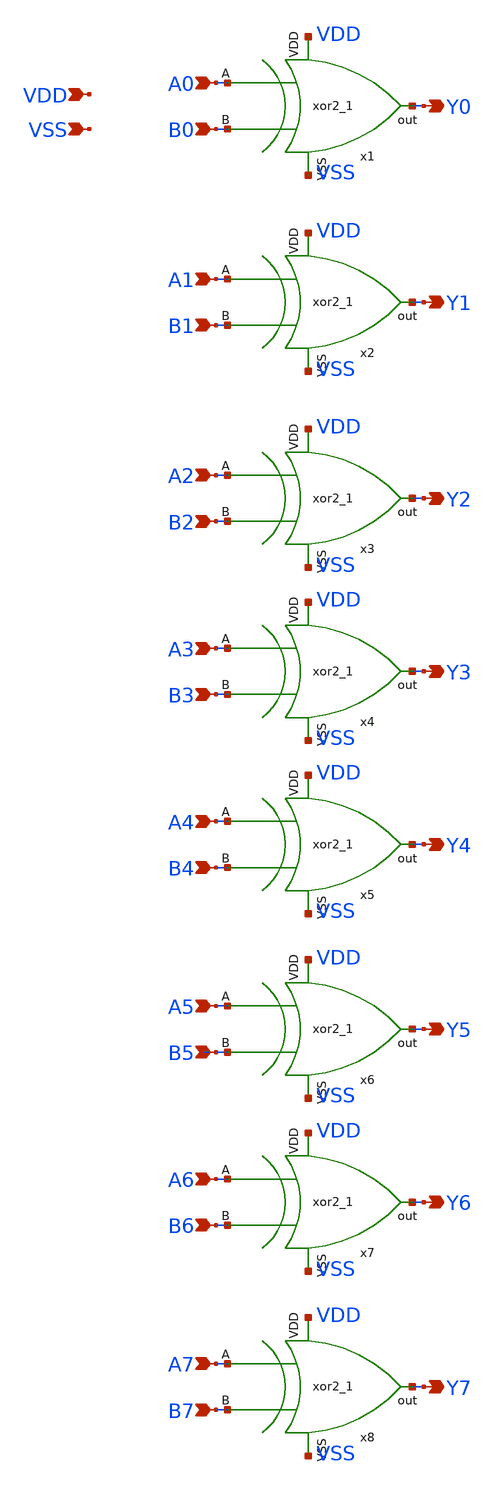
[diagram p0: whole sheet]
** sch_path: xor2/xor2_8bit.sch
**.subckt xor2_8bit A0 B0 A1 B1 A2 B2 A3 B3 A4 B4 A5 B5 A6 B6 A7 B7 Y7 Y6 Y5 Y4 Y3 Y2 Y1 Y0 VDD VSS
*.ipin A0
*.ipin B0
*.ipin A1
*.ipin B1
*.ipin A2
*.ipin B2
*.ipin A3
*.ipin B3
*.ipin A4
*.ipin B4
*.ipin A5
*.ipin B5
*.ipin A6
*.ipin B6
*.ipin A7
*.ipin B7
*.opin Y7
*.opin Y6
*.opin Y5
*.opin Y4
*.opin Y3
*.opin Y2
*.opin Y1
*.opin Y0
*.ipin VDD
*.ipin VSS
x1 A0 B0 VDD VSS Y0 xor2
x2 A1 B1 VDD VSS Y1 xor2
x3 A2 B2 VDD VSS Y2 xor2
x4 A3 B3 VDD VSS Y3 xor2
x5 A4 B4 VDD VSS Y4 xor2
x6 A5 B5 VDD VSS Y5 xor2
x7 A6 B6 VDD VSS Y6 xor2
x8 A7 B7 VDD VSS Y7 xor2
**.ends

* expanding   symbol:  xor2/xor2.sym # of pins=5
** sym_path: xor2/xor2.sym
** sch_path: xor2/xor2.sch
.subckt xor2 A B VDD VSS out
*.ipin A
*.ipin B
*.opin out
*.ipin VDD
*.ipin VSS
XM1 out notA net3 net3 sky130_fd_pr__nfet_01v8 L=0.15 W=1 nf=1 ad='int((nf+1)/2) * W/nf * 0.29' as='int((nf+2)/2) * W/nf * 0.29'
+ pd='2*int((nf+1)/2) * (W/nf + 0.29)' ps='2*int((nf+2)/2) * (W/nf + 0.29)' nrd='0.29 / W' nrs='0.29 / W'
+ sa=0 sb=0 sd=0 mult=1 m=1
XM2 out B net1 net1 sky130_fd_pr__pfet_01v8 L=0.15 W=1 nf=1 ad='int((nf+1)/2) * W/nf * 0.29' as='int((nf+2)/2) * W/nf * 0.29'
+ pd='2*int((nf+1)/2) * (W/nf + 0.29)' ps='2*int((nf+2)/2) * (W/nf + 0.29)' nrd='0.29 / W' nrs='0.29 / W'
+ sa=0 sb=0 sd=0 mult=1 m=1
XM3 net3 notB VSS VSS sky130_fd_pr__nfet_01v8 L=0.15 W=1 nf=1 ad='int((nf+1)/2) * W/nf * 0.29' as='int((nf+2)/2) * W/nf * 0.29'
+ pd='2*int((nf+1)/2) * (W/nf + 0.29)' ps='2*int((nf+2)/2) * (W/nf + 0.29)' nrd='0.29 / W' nrs='0.29 / W'
+ sa=0 sb=0 sd=0 mult=1 m=1
XM4 net1 notA VDD VDD sky130_fd_pr__pfet_01v8 L=0.15 W=1 nf=1 ad='int((nf+1)/2) * W/nf * 0.29' as='int((nf+2)/2) * W/nf * 0.29'
+ pd='2*int((nf+1)/2) * (W/nf + 0.29)' ps='2*int((nf+2)/2) * (W/nf + 0.29)' nrd='0.29 / W' nrs='0.29 / W'
+ sa=0 sb=0 sd=0 mult=1 m=1
XM5 net4 A VDD VDD sky130_fd_pr__pfet_01v8 L=0.15 W=1 nf=1 ad='int((nf+1)/2) * W/nf * 0.29' as='int((nf+2)/2) * W/nf * 0.29'
+ pd='2*int((nf+1)/2) * (W/nf + 0.29)' ps='2*int((nf+2)/2) * (W/nf + 0.29)' nrd='0.29 / W' nrs='0.29 / W'
+ sa=0 sb=0 sd=0 mult=1 m=1
XM6 out notB net4 net4 sky130_fd_pr__pfet_01v8 L=0.15 W=1 nf=1 ad='int((nf+1)/2) * W/nf * 0.29' as='int((nf+2)/2) * W/nf * 0.29'
+ pd='2*int((nf+1)/2) * (W/nf + 0.29)' ps='2*int((nf+2)/2) * (W/nf + 0.29)' nrd='0.29 / W' nrs='0.29 / W'
+ sa=0 sb=0 sd=0 mult=1 m=1
XM7 out A net2 net2 sky130_fd_pr__nfet_01v8 L=0.15 W=1 nf=1 ad='int((nf+1)/2) * W/nf * 0.29' as='int((nf+2)/2) * W/nf * 0.29'
+ pd='2*int((nf+1)/2) * (W/nf + 0.29)' ps='2*int((nf+2)/2) * (W/nf + 0.29)' nrd='0.29 / W' nrs='0.29 / W'
+ sa=0 sb=0 sd=0 mult=1 m=1
XM8 net2 B VSS VSS sky130_fd_pr__nfet_01v8 L=0.15 W=1 nf=1 ad='int((nf+1)/2) * W/nf * 0.29' as='int((nf+2)/2) * W/nf * 0.29'
+ pd='2*int((nf+1)/2) * (W/nf + 0.29)' ps='2*int((nf+2)/2) * (W/nf + 0.29)' nrd='0.29 / W' nrs='0.29 / W'
+ sa=0 sb=0 sd=0 mult=1 m=1
XM9 notA A VDD VDD sky130_fd_pr__pfet_01v8 L=0.15 W=1 nf=1 ad='int((nf+1)/2) * W/nf * 0.29' as='int((nf+2)/2) * W/nf * 0.29'
+ pd='2*int((nf+1)/2) * (W/nf + 0.29)' ps='2*int((nf+2)/2) * (W/nf + 0.29)' nrd='0.29 / W' nrs='0.29 / W'
+ sa=0 sb=0 sd=0 mult=1 m=1
XM10 notA A VSS VSS sky130_fd_pr__nfet_01v8 L=0.15 W=1 nf=1 ad='int((nf+1)/2) * W/nf * 0.29' as='int((nf+2)/2) * W/nf * 0.29'
+ pd='2*int((nf+1)/2) * (W/nf + 0.29)' ps='2*int((nf+2)/2) * (W/nf + 0.29)' nrd='0.29 / W' nrs='0.29 / W'
+ sa=0 sb=0 sd=0 mult=1 m=1
XM11 notB B VDD VDD sky130_fd_pr__pfet_01v8 L=0.15 W=1 nf=1 ad='int((nf+1)/2) * W/nf * 0.29' as='int((nf+2)/2) * W/nf * 0.29'
+ pd='2*int((nf+1)/2) * (W/nf + 0.29)' ps='2*int((nf+2)/2) * (W/nf + 0.29)' nrd='0.29 / W' nrs='0.29 / W'
+ sa=0 sb=0 sd=0 mult=1 m=1
XM12 notB B VSS VSS sky130_fd_pr__nfet_01v8 L=0.15 W=1 nf=1 ad='int((nf+1)/2) * W/nf * 0.29' as='int((nf+2)/2) * W/nf * 0.29'
+ pd='2*int((nf+1)/2) * (W/nf + 0.29)' ps='2*int((nf+2)/2) * (W/nf + 0.29)' nrd='0.29 / W' nrs='0.29 / W'
+ sa=0 sb=0 sd=0 mult=1 m=1
.ends

.end
